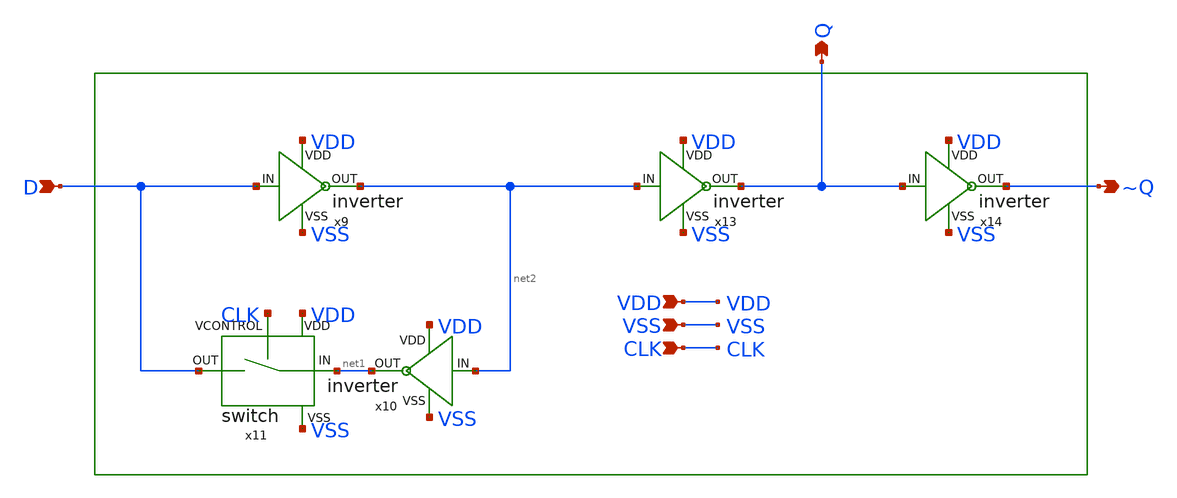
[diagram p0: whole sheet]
** sch_path: d-flip-flop/d_flipflop.sch
**.subckt d_flipflop CLK VDD VSS D Q ~Q
*.ipin CLK
*.ipin VDD
*.ipin VSS
*.ipin D
*.opin Q
*.opin ~Q
x9 VDD D net2 VSS inverter
x10 VDD net2 net1 VSS inverter
x11 D net1 VDD CLK VSS switch
x13 VDD net2 Q VSS inverter
x14 VDD Q ~Q VSS inverter
**.ends
.end
